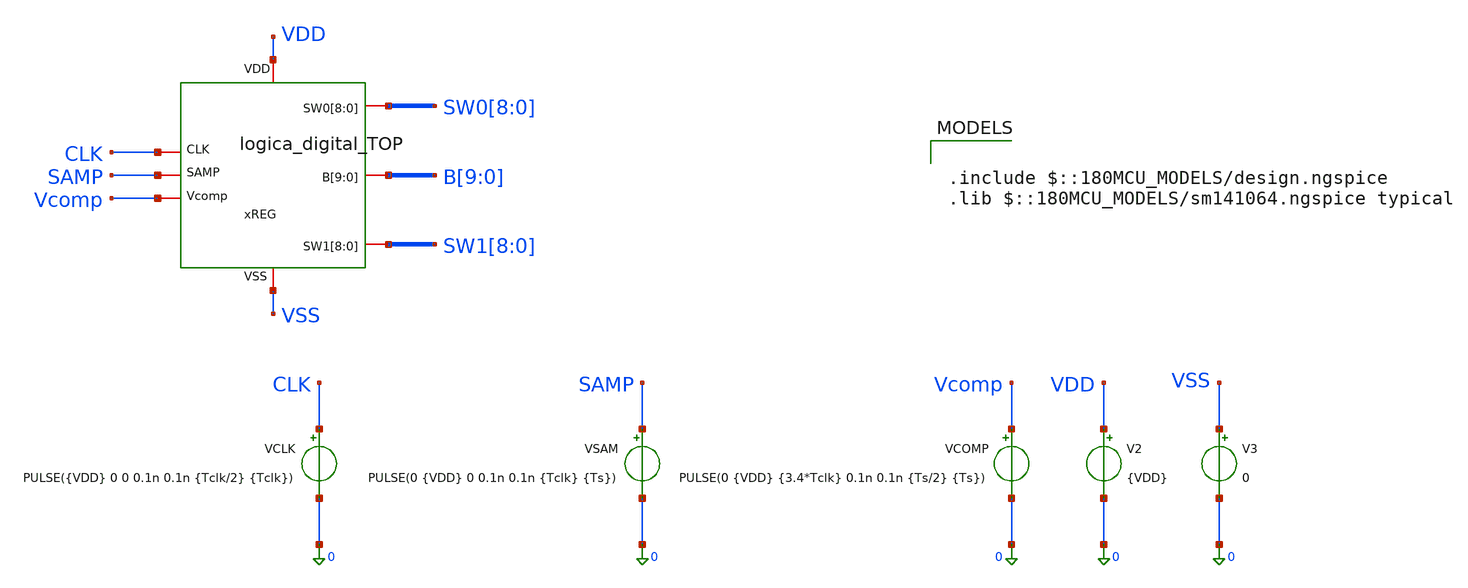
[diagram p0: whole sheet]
** sch_path: designs/sar_adc/digital/logica_digital_TOP/xschem/logica_digital_TOP_tb.sch
**.subckt logica_digital_TOP_tb
xREG VDD CLK SAMP Vcomp SW0[8] SW0[7] SW0[6] SW0[5] SW0[4] SW0[3] SW0[2] SW0[1] SW0[0] B[9] B[8]
+ B[7] B[6] B[5] B[4] B[3] B[2] B[1] B[0] SW1[8] SW1[7] SW1[6] SW1[5] SW1[4] SW1[3] SW1[2] SW1[1] SW1[0]
+ VSS logica_digital_TOP
V2 VDD 0 {VDD}
V3 VSS 0 0
VCOMP Vcomp 0 PULSE(0 {VDD} {3.4*Tclk} 0.1n 0.1n {Ts/2} {Ts})
VCLK CLK 0 PULSE({VDD} 0 0 0.1n 0.1n {Tclk/2} {Tclk})
VSAM SAMP 0 PULSE(0 {VDD} 0 0.1n 0.1n {Tclk} {Ts})
**** begin user architecture code

.include $::180MCU_MODELS/design.ngspice
.lib $::180MCU_MODELS/sm141064.ngspice typical



* Input parameters
.param VDD = 3.3
.param Fs = 5Meg
.param Ts = 1/Fs
.param Tclk = 1/(Fs*12)

.control
save all

* Variables
let Fs = 5Meg
let tstep = 1/(Fs*12*100)
let tstop = 2/Fs


* Transient simulation
tran $&tstep $&tstop

let i_vdd = -i(V2)
let p_inst = -v(VDD)*i(V2)
** Plots
meas tran Iavg AVG i_vdd FROM=$&tstep TO=$&tstop
meas tran Pavg AVG p_inst FROM=$&tstep TO=$&tstop

*plot xREG.SAMPN xREG.SET

plot "sw0[8]" "sw0[7]" "sw0[6]" "sw1[8]"+4 "sw1[7]"+4 "sw1[6]"+4
.endc


**** end user architecture code
**.ends
.end
